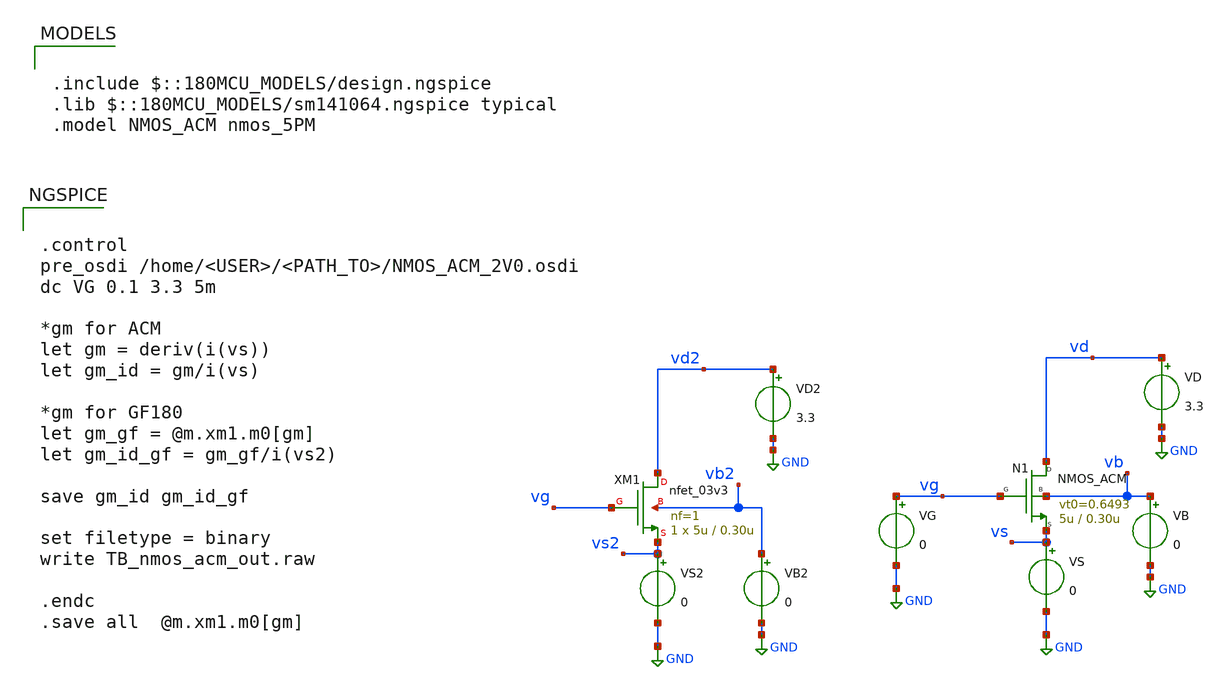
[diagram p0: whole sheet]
** sch_path: legacy/Examples/SkyWater130/xschem/TB_nmos_acm.sch
**.subckt TB_nmos_acm
VG vg GND 0
VD vd GND 3.3
VB vb GND 0
VS vs GND 0
N1 vd vg vs vb NMOS_ACM w=5u l=0.30u n=1.383 is=1.076u vt0=0.6493 sigma=26m zeta=22m
XM1 vd2 vg vs2 vb2 nfet_03v3 L=0.30u W=5u nf=1 ad='int((nf+1)/2) * W/nf * 0.18u' as='int((nf+2)/2) * W/nf * 0.18u'
+ pd='2*int((nf+1)/2) * (W/nf + 0.18u)' ps='2*int((nf+2)/2) * (W/nf + 0.18u)' nrd='0.18u / W' nrs='0.18u / W'
+ sa=0 sb=0 sd=0 m=1
VD2 vd2 GND 3.3
VB2 vb2 GND 0
VS2 vs2 GND 0
**** begin user architecture code

.include $::180MCU_MODELS/design.ngspice
.lib $::180MCU_MODELS/sm141064.ngspice typical
.model NMOS_ACM nmos_5PM



.control
pre_osdi /home/<USER>/<PATH_TO>/NMOS_ACM_2V0.osdi
dc VG 0.1 3.3 5m

*gm for ACM
let gm = deriv(i(vs))
let gm_id = gm/i(vs)

*gm for GF180
let gm_gf = @m.xm1.m0[gm]
let gm_id_gf = gm_gf/i(vs2)

save gm_id gm_id_gf

set filetype = binary
write TB_nmos_acm_out.raw

.endc
.save all  @m.xm1.m0[gm]


**** end user architecture code
**.ends
.GLOBAL GND
.end
